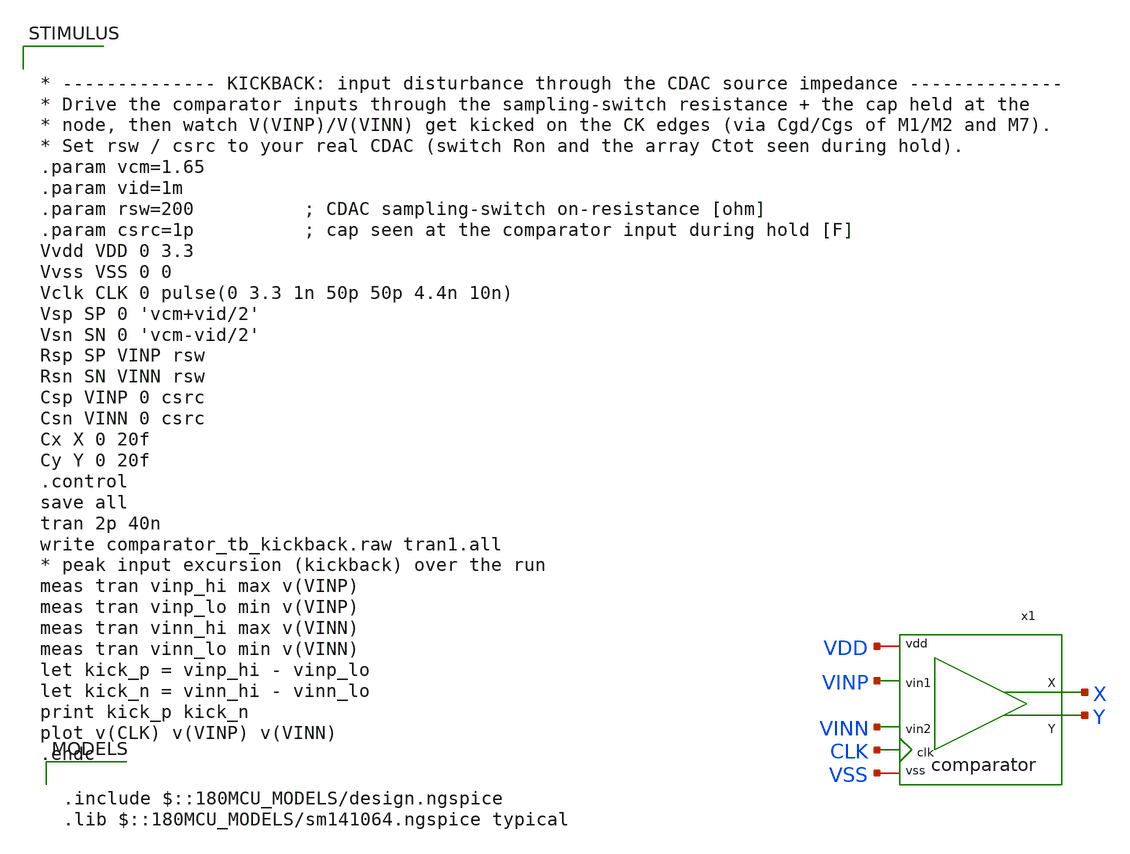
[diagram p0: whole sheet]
** sch_path: designs/libs/core_analog/saradc/tb/comparator_tb_kickback.sch
**.subckt comparator_tb_kickback
x1 VDD VSS X VINP Y VINN CLK comparator
**** begin user architecture code

.include $::180MCU_MODELS/design.ngspice
.lib $::180MCU_MODELS/sm141064.ngspice typical



* -------------- KICKBACK: input disturbance through the CDAC source impedance --------------
* Drive the comparator inputs through the sampling-switch resistance + the cap held at the
* node, then watch V(VINP)/V(VINN) get kicked on the CK edges (via Cgd/Cgs of M1/M2 and M7).
* Set rsw / csrc to your real CDAC (switch Ron and the array Ctot seen during hold).
.param vcm=1.65
.param vid=1m
.param rsw=200          ; CDAC sampling-switch on-resistance [ohm]
.param csrc=1p          ; cap seen at the comparator input during hold [F]
Vvdd VDD 0 3.3
Vvss VSS 0 0
Vclk CLK 0 pulse(0 3.3 1n 50p 50p 4.4n 10n)
Vsp SP 0 'vcm+vid/2'
Vsn SN 0 'vcm-vid/2'
Rsp SP VINP rsw
Rsn SN VINN rsw
Csp VINP 0 csrc
Csn VINN 0 csrc
Cx X 0 20f
Cy Y 0 20f
.control
save all
tran 2p 40n
write comparator_tb_kickback.raw tran1.all
* peak input excursion (kickback) over the run
meas tran vinp_hi max v(VINP)
meas tran vinp_lo min v(VINP)
meas tran vinn_hi max v(VINN)
meas tran vinn_lo min v(VINN)
let kick_p = vinp_hi - vinp_lo
let kick_n = vinn_hi - vinn_lo
print kick_p kick_n
plot v(CLK) v(VINP) v(VINN)
.endc


**** end user architecture code
**.ends

* expanding   symbol:  comparator.sym # of pins=7
** sym_path: designs/libs/core_analog/saradc/comparator.sym
** sch_path: designs/libs/core_analog/saradc/comparator.sch
.subckt comparator vdd vss X vin1 Y vin2 clk
*.iopin vdd
*.iopin vss
*.ipin vin1
*.ipin vin2
*.ipin clk
*.opin X
*.opin Y
XM1 P vin1 net1 vss nfet_03v3 L=0.5u W=4u nf=4 ad='int((nf+1)/2) * W/nf * 0.18u' as='int((nf+2)/2) * W/nf * 0.18u'
+ pd='2*int((nf+1)/2) * (W/nf + 0.18u)' ps='2*int((nf+2)/2) * (W/nf + 0.18u)' nrd='0.18u / W' nrs='0.18u / W'
+ sa=0 sb=0 sd=0 m=1
XM2 Q vin2 net1 vss nfet_03v3 L=0.5u W=4u nf=4 ad='int((nf+1)/2) * W/nf * 0.18u' as='int((nf+2)/2) * W/nf * 0.18u'
+ pd='2*int((nf+1)/2) * (W/nf + 0.18u)' ps='2*int((nf+2)/2) * (W/nf + 0.18u)' nrd='0.18u / W' nrs='0.18u / W'
+ sa=0 sb=0 sd=0 m=1
XM3 X Y P vss nfet_03v3 L=0.28u W=2u nf=2 ad='int((nf+1)/2) * W/nf * 0.18u' as='int((nf+2)/2) * W/nf * 0.18u'
+ pd='2*int((nf+1)/2) * (W/nf + 0.18u)' ps='2*int((nf+2)/2) * (W/nf + 0.18u)' nrd='0.18u / W' nrs='0.18u / W'
+ sa=0 sb=0 sd=0 m=1
XM4 Y X Q vss nfet_03v3 L=0.28u W=2u nf=2 ad='int((nf+1)/2) * W/nf * 0.18u' as='int((nf+2)/2) * W/nf * 0.18u'
+ pd='2*int((nf+1)/2) * (W/nf + 0.18u)' ps='2*int((nf+2)/2) * (W/nf + 0.18u)' nrd='0.18u / W' nrs='0.18u / W'
+ sa=0 sb=0 sd=0 m=1
XM5 X Y vdd vdd pfet_03v3 L=0.28u W=6u nf=2 ad='int((nf+1)/2) * W/nf * 0.18u' as='int((nf+2)/2) * W/nf * 0.18u'
+ pd='2*int((nf+1)/2) * (W/nf + 0.18u)' ps='2*int((nf+2)/2) * (W/nf + 0.18u)' nrd='0.18u / W' nrs='0.18u / W'
+ sa=0 sb=0 sd=0 m=1
XM6 Y X vdd vdd pfet_03v3 L=0.28u W=6u nf=2 ad='int((nf+1)/2) * W/nf * 0.18u' as='int((nf+2)/2) * W/nf * 0.18u'
+ pd='2*int((nf+1)/2) * (W/nf + 0.18u)' ps='2*int((nf+2)/2) * (W/nf + 0.18u)' nrd='0.18u / W' nrs='0.18u / W'
+ sa=0 sb=0 sd=0 m=1
XM7 net1 clk vss vss nfet_03v3 L=0.28u W=6u nf=4 ad='int((nf+1)/2) * W/nf * 0.18u' as='int((nf+2)/2) * W/nf * 0.18u'
+ pd='2*int((nf+1)/2) * (W/nf + 0.18u)' ps='2*int((nf+2)/2) * (W/nf + 0.18u)' nrd='0.18u / W' nrs='0.18u / W'
+ sa=0 sb=0 sd=0 m=1
XM8 X clk vdd vdd pfet_03v3 L=0.28u W=2u nf=1 ad='int((nf+1)/2) * W/nf * 0.18u' as='int((nf+2)/2) * W/nf * 0.18u'
+ pd='2*int((nf+1)/2) * (W/nf + 0.18u)' ps='2*int((nf+2)/2) * (W/nf + 0.18u)' nrd='0.18u / W' nrs='0.18u / W'
+ sa=0 sb=0 sd=0 m=1
XM9 P clk vdd vdd pfet_03v3 L=0.28u W=2u nf=1 ad='int((nf+1)/2) * W/nf * 0.18u' as='int((nf+2)/2) * W/nf * 0.18u'
+ pd='2*int((nf+1)/2) * (W/nf + 0.18u)' ps='2*int((nf+2)/2) * (W/nf + 0.18u)' nrd='0.18u / W' nrs='0.18u / W'
+ sa=0 sb=0 sd=0 m=1
XM10 Y clk vdd vdd pfet_03v3 L=0.28u W=2u nf=1 ad='int((nf+1)/2) * W/nf * 0.18u' as='int((nf+2)/2) * W/nf * 0.18u'
+ pd='2*int((nf+1)/2) * (W/nf + 0.18u)' ps='2*int((nf+2)/2) * (W/nf + 0.18u)' nrd='0.18u / W' nrs='0.18u / W'
+ sa=0 sb=0 sd=0 m=1
XM11 Q clk vdd vdd pfet_03v3 L=0.28u W=2u nf=1 ad='int((nf+1)/2) * W/nf * 0.18u' as='int((nf+2)/2) * W/nf * 0.18u'
+ pd='2*int((nf+1)/2) * (W/nf + 0.18u)' ps='2*int((nf+2)/2) * (W/nf + 0.18u)' nrd='0.18u / W' nrs='0.18u / W'
+ sa=0 sb=0 sd=0 m=1
.ends

.end
